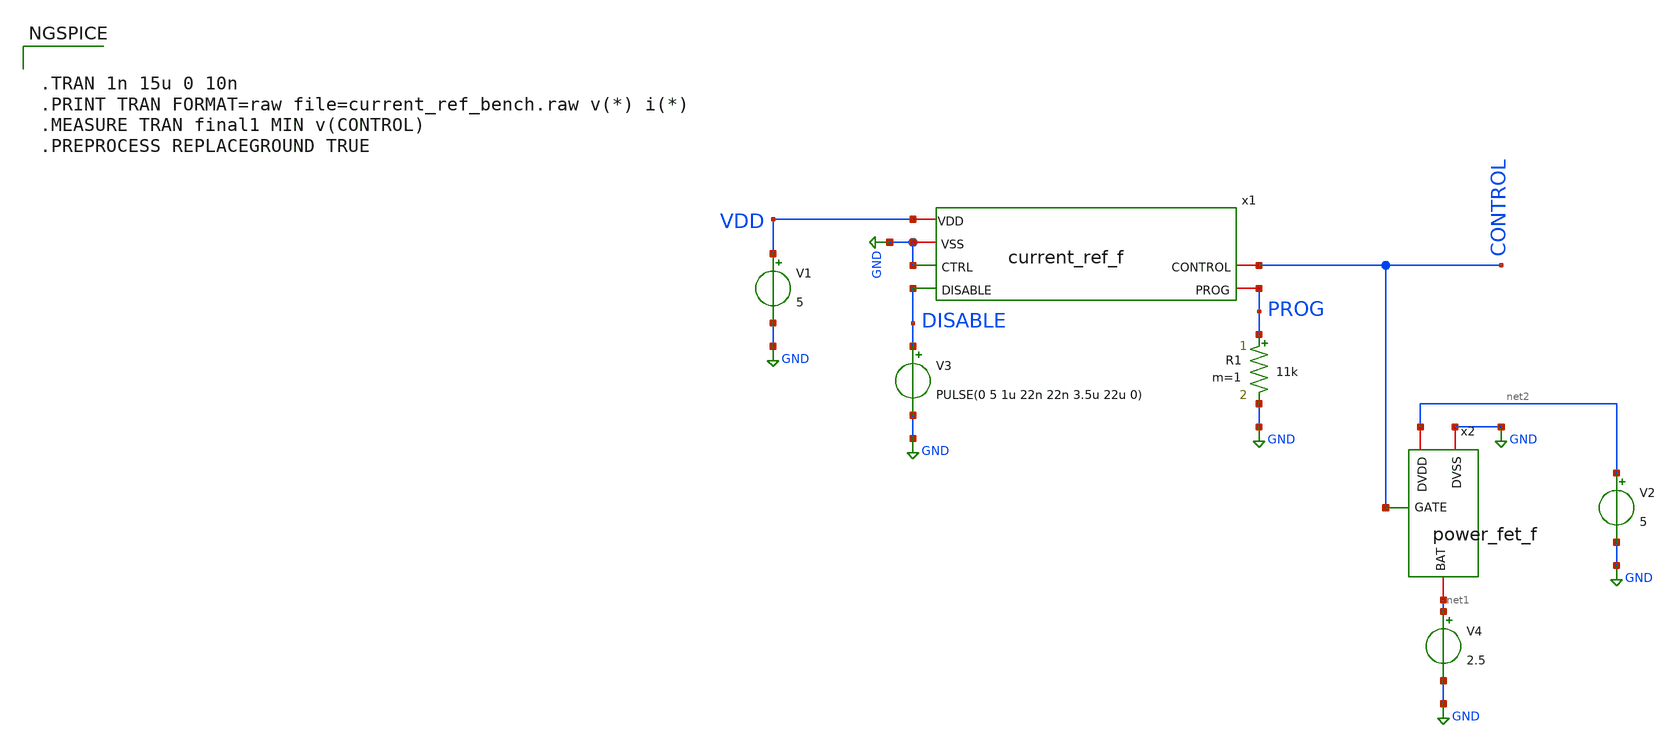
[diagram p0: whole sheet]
** sch_path: analog/xschem/current_ref_bench.sch
**.subckt current_ref_bench
V1 VDD GND 5
V4 net1 GND 2.5
V2 net2 GND 5
R1 PROG GND 11k m=1
V3 DISABLE GND PULSE(0 5 1u 22n 22n 3.5u 22u 0)
x1 VDD GND GND DISABLE CONTROL PROG current_ref_f
x2 net2 GND net1 CONTROL power_fet_f
**** begin user architecture code


.TRAN 1n 15u 0 10n
.PRINT TRAN FORMAT=raw file=current_ref_bench.raw v(*) i(*)
.MEASURE TRAN final1 MIN v(CONTROL)
.PREPROCESS REPLACEGROUND TRUE



.include $::PDK_ROOT/gf180mcuD/libs.tech/xyce/design.xyce
.lib $::PDK_ROOT/gf180mcuD/libs.tech/xyce/sm141064.xyce typical
.lib $::PDK_ROOT/gf180mcuD/libs.tech/xyce/sm141064.xyce res_typical
.lib $::PDK_ROOT/gf180mcuD/libs.tech/xyce/sm141064.xyce diode_typical
.lib $::PDK_ROOT/gf180mcuD/libs.tech/xyce/sm141064.xyce mimcap_typical
.lib $::PDK_ROOT/gf180mcuD/libs.tech/xyce/sm141064.xyce cap_mim
.include /foss/designs/charger/xschem/extracted/current_ref_f.spice
.include /foss/designs/charger/xschem/extracted/power_fet_f.spice

**** end user architecture code
**.ends
.GLOBAL GND
.end
